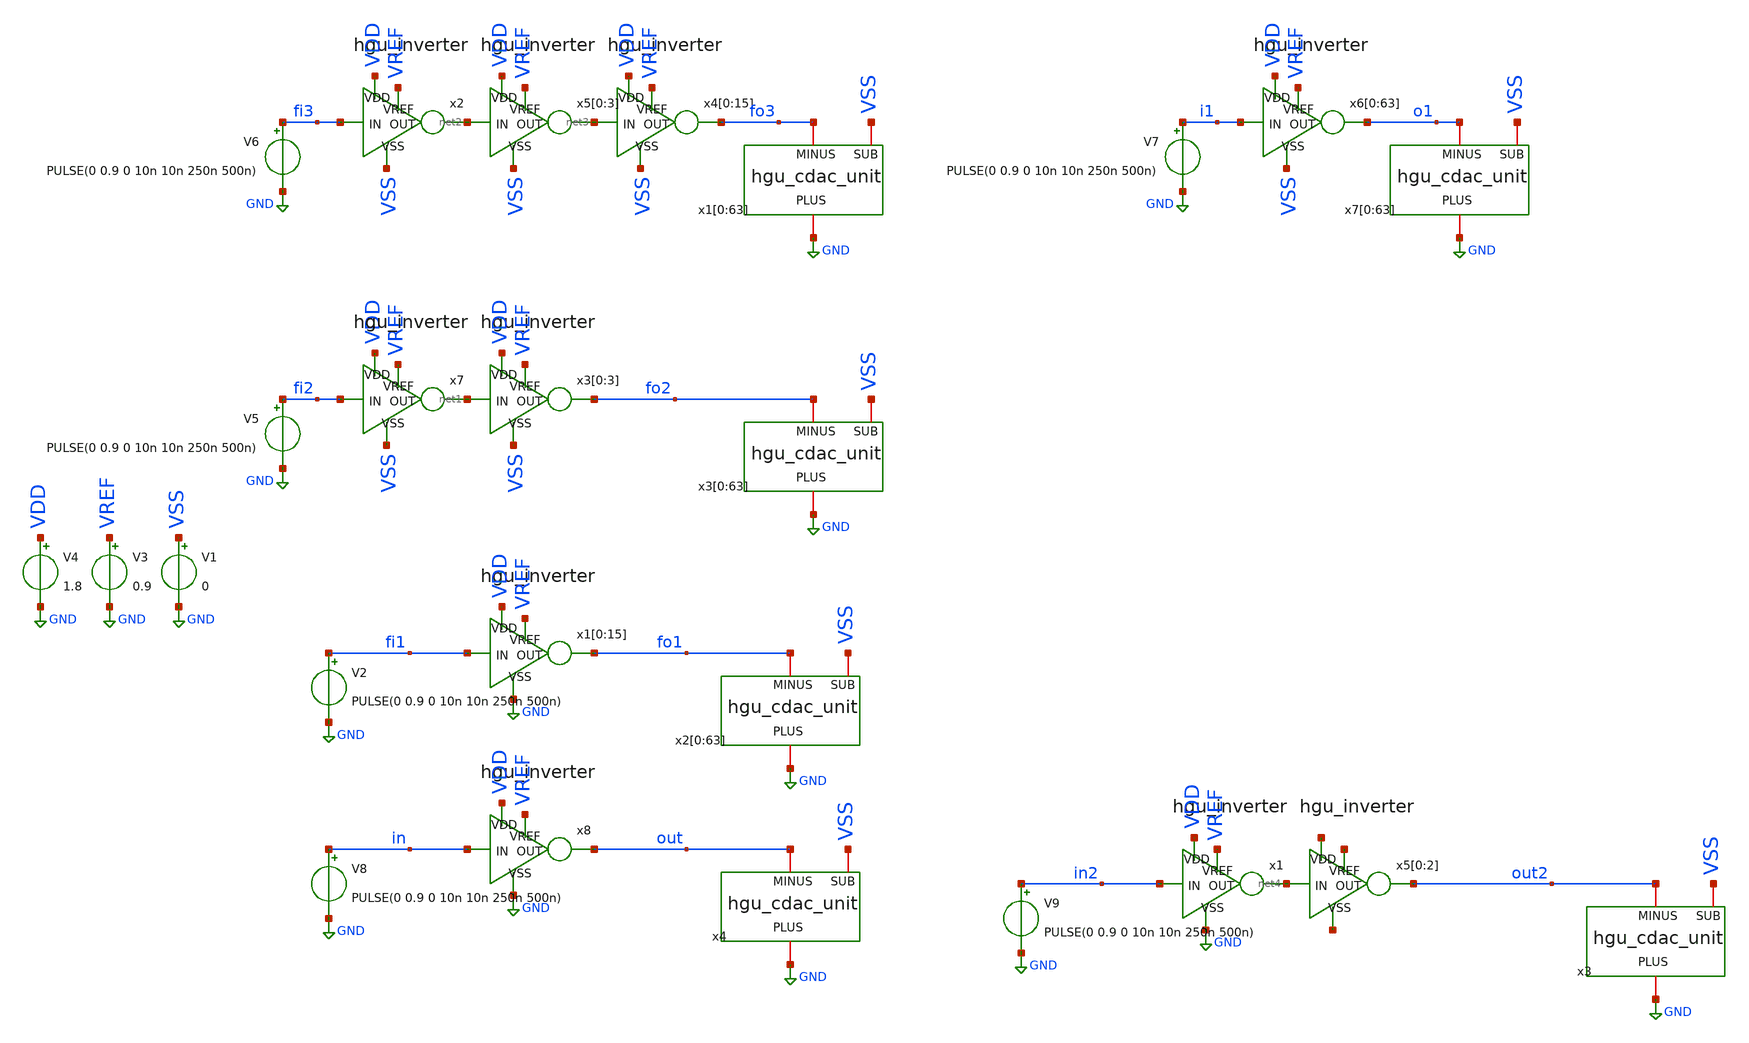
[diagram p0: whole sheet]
** sch_path: hgu/tb/tb_hgu_cdac_drv.sch
**.subckt tb_hgu_cdac_drv
x1[0] VDD fi1 fo1 GND VREF hgu_inverter
x1[1] VDD fi1 fo1 GND VREF hgu_inverter
x1[2] VDD fi1 fo1 GND VREF hgu_inverter
x1[3] VDD fi1 fo1 GND VREF hgu_inverter
x1[4] VDD fi1 fo1 GND VREF hgu_inverter
x1[5] VDD fi1 fo1 GND VREF hgu_inverter
x1[6] VDD fi1 fo1 GND VREF hgu_inverter
x1[7] VDD fi1 fo1 GND VREF hgu_inverter
x1[8] VDD fi1 fo1 GND VREF hgu_inverter
x1[9] VDD fi1 fo1 GND VREF hgu_inverter
x1[10] VDD fi1 fo1 GND VREF hgu_inverter
x1[11] VDD fi1 fo1 GND VREF hgu_inverter
x1[12] VDD fi1 fo1 GND VREF hgu_inverter
x1[13] VDD fi1 fo1 GND VREF hgu_inverter
x1[14] VDD fi1 fo1 GND VREF hgu_inverter
x1[15] VDD fi1 fo1 GND VREF hgu_inverter
x2[0] GND fo1 VSS hgu_cdac_unit
x2[1] GND fo1 VSS hgu_cdac_unit
x2[2] GND fo1 VSS hgu_cdac_unit
x2[3] GND fo1 VSS hgu_cdac_unit
x2[4] GND fo1 VSS hgu_cdac_unit
x2[5] GND fo1 VSS hgu_cdac_unit
x2[6] GND fo1 VSS hgu_cdac_unit
x2[7] GND fo1 VSS hgu_cdac_unit
x2[8] GND fo1 VSS hgu_cdac_unit
x2[9] GND fo1 VSS hgu_cdac_unit
x2[10] GND fo1 VSS hgu_cdac_unit
x2[11] GND fo1 VSS hgu_cdac_unit
x2[12] GND fo1 VSS hgu_cdac_unit
x2[13] GND fo1 VSS hgu_cdac_unit
x2[14] GND fo1 VSS hgu_cdac_unit
x2[15] GND fo1 VSS hgu_cdac_unit
x2[16] GND fo1 VSS hgu_cdac_unit
x2[17] GND fo1 VSS hgu_cdac_unit
x2[18] GND fo1 VSS hgu_cdac_unit
x2[19] GND fo1 VSS hgu_cdac_unit
x2[20] GND fo1 VSS hgu_cdac_unit
x2[21] GND fo1 VSS hgu_cdac_unit
x2[22] GND fo1 VSS hgu_cdac_unit
x2[23] GND fo1 VSS hgu_cdac_unit
x2[24] GND fo1 VSS hgu_cdac_unit
x2[25] GND fo1 VSS hgu_cdac_unit
x2[26] GND fo1 VSS hgu_cdac_unit
x2[27] GND fo1 VSS hgu_cdac_unit
x2[28] GND fo1 VSS hgu_cdac_unit
x2[29] GND fo1 VSS hgu_cdac_unit
x2[30] GND fo1 VSS hgu_cdac_unit
x2[31] GND fo1 VSS hgu_cdac_unit
x2[32] GND fo1 VSS hgu_cdac_unit
x2[33] GND fo1 VSS hgu_cdac_unit
x2[34] GND fo1 VSS hgu_cdac_unit
x2[35] GND fo1 VSS hgu_cdac_unit
x2[36] GND fo1 VSS hgu_cdac_unit
x2[37] GND fo1 VSS hgu_cdac_unit
x2[38] GND fo1 VSS hgu_cdac_unit
x2[39] GND fo1 VSS hgu_cdac_unit
x2[40] GND fo1 VSS hgu_cdac_unit
x2[41] GND fo1 VSS hgu_cdac_unit
x2[42] GND fo1 VSS hgu_cdac_unit
x2[43] GND fo1 VSS hgu_cdac_unit
x2[44] GND fo1 VSS hgu_cdac_unit
x2[45] GND fo1 VSS hgu_cdac_unit
x2[46] GND fo1 VSS hgu_cdac_unit
x2[47] GND fo1 VSS hgu_cdac_unit
x2[48] GND fo1 VSS hgu_cdac_unit
x2[49] GND fo1 VSS hgu_cdac_unit
x2[50] GND fo1 VSS hgu_cdac_unit
x2[51] GND fo1 VSS hgu_cdac_unit
x2[52] GND fo1 VSS hgu_cdac_unit
x2[53] GND fo1 VSS hgu_cdac_unit
x2[54] GND fo1 VSS hgu_cdac_unit
x2[55] GND fo1 VSS hgu_cdac_unit
x2[56] GND fo1 VSS hgu_cdac_unit
x2[57] GND fo1 VSS hgu_cdac_unit
x2[58] GND fo1 VSS hgu_cdac_unit
x2[59] GND fo1 VSS hgu_cdac_unit
x2[60] GND fo1 VSS hgu_cdac_unit
x2[61] GND fo1 VSS hgu_cdac_unit
x2[62] GND fo1 VSS hgu_cdac_unit
x2[63] GND fo1 VSS hgu_cdac_unit
V1 VSS GND 0
V2 fi1 GND PULSE(0 0.9 0 10n 10n 250n 500n)
V3 VREF GND 0.9
V4 VDD GND 1.8
x3[0] VDD net1 fo2 VSS VREF hgu_inverter
x3[1] VDD net1 fo2 VSS VREF hgu_inverter
x3[2] VDD net1 fo2 VSS VREF hgu_inverter
x3[3] VDD net1 fo2 VSS VREF hgu_inverter
x3[0] GND fo2 VSS hgu_cdac_unit
x3[1] GND fo2 VSS hgu_cdac_unit
x3[2] GND fo2 VSS hgu_cdac_unit
x3[3] GND fo2 VSS hgu_cdac_unit
x3[4] GND fo2 VSS hgu_cdac_unit
x3[5] GND fo2 VSS hgu_cdac_unit
x3[6] GND fo2 VSS hgu_cdac_unit
x3[7] GND fo2 VSS hgu_cdac_unit
x3[8] GND fo2 VSS hgu_cdac_unit
x3[9] GND fo2 VSS hgu_cdac_unit
x3[10] GND fo2 VSS hgu_cdac_unit
x3[11] GND fo2 VSS hgu_cdac_unit
x3[12] GND fo2 VSS hgu_cdac_unit
x3[13] GND fo2 VSS hgu_cdac_unit
x3[14] GND fo2 VSS hgu_cdac_unit
x3[15] GND fo2 VSS hgu_cdac_unit
x3[16] GND fo2 VSS hgu_cdac_unit
x3[17] GND fo2 VSS hgu_cdac_unit
x3[18] GND fo2 VSS hgu_cdac_unit
x3[19] GND fo2 VSS hgu_cdac_unit
x3[20] GND fo2 VSS hgu_cdac_unit
x3[21] GND fo2 VSS hgu_cdac_unit
x3[22] GND fo2 VSS hgu_cdac_unit
x3[23] GND fo2 VSS hgu_cdac_unit
x3[24] GND fo2 VSS hgu_cdac_unit
x3[25] GND fo2 VSS hgu_cdac_unit
x3[26] GND fo2 VSS hgu_cdac_unit
x3[27] GND fo2 VSS hgu_cdac_unit
x3[28] GND fo2 VSS hgu_cdac_unit
x3[29] GND fo2 VSS hgu_cdac_unit
x3[30] GND fo2 VSS hgu_cdac_unit
x3[31] GND fo2 VSS hgu_cdac_unit
x3[32] GND fo2 VSS hgu_cdac_unit
x3[33] GND fo2 VSS hgu_cdac_unit
x3[34] GND fo2 VSS hgu_cdac_unit
x3[35] GND fo2 VSS hgu_cdac_unit
x3[36] GND fo2 VSS hgu_cdac_unit
x3[37] GND fo2 VSS hgu_cdac_unit
x3[38] GND fo2 VSS hgu_cdac_unit
x3[39] GND fo2 VSS hgu_cdac_unit
x3[40] GND fo2 VSS hgu_cdac_unit
x3[41] GND fo2 VSS hgu_cdac_unit
x3[42] GND fo2 VSS hgu_cdac_unit
x3[43] GND fo2 VSS hgu_cdac_unit
x3[44] GND fo2 VSS hgu_cdac_unit
x3[45] GND fo2 VSS hgu_cdac_unit
x3[46] GND fo2 VSS hgu_cdac_unit
x3[47] GND fo2 VSS hgu_cdac_unit
x3[48] GND fo2 VSS hgu_cdac_unit
x3[49] GND fo2 VSS hgu_cdac_unit
x3[50] GND fo2 VSS hgu_cdac_unit
x3[51] GND fo2 VSS hgu_cdac_unit
x3[52] GND fo2 VSS hgu_cdac_unit
x3[53] GND fo2 VSS hgu_cdac_unit
x3[54] GND fo2 VSS hgu_cdac_unit
x3[55] GND fo2 VSS hgu_cdac_unit
x3[56] GND fo2 VSS hgu_cdac_unit
x3[57] GND fo2 VSS hgu_cdac_unit
x3[58] GND fo2 VSS hgu_cdac_unit
x3[59] GND fo2 VSS hgu_cdac_unit
x3[60] GND fo2 VSS hgu_cdac_unit
x3[61] GND fo2 VSS hgu_cdac_unit
x3[62] GND fo2 VSS hgu_cdac_unit
x3[63] GND fo2 VSS hgu_cdac_unit
V5 fi2 GND PULSE(0 0.9 0 10n 10n 250n 500n)
x5[0] VDD net2 net3[3] VSS VREF hgu_inverter
x5[1] VDD net2 net3[2] VSS VREF hgu_inverter
x5[2] VDD net2 net3[1] VSS VREF hgu_inverter
x5[3] VDD net2 net3[0] VSS VREF hgu_inverter
x2 VDD fi3 net2 VSS VREF hgu_inverter
x4[0] VDD net3[3] fo3 VSS VREF hgu_inverter
x4[1] VDD net3[2] fo3 VSS VREF hgu_inverter
x4[2] VDD net3[1] fo3 VSS VREF hgu_inverter
x4[3] VDD net3[0] fo3 VSS VREF hgu_inverter
x4[4] VDD net3[3] fo3 VSS VREF hgu_inverter
x4[5] VDD net3[2] fo3 VSS VREF hgu_inverter
x4[6] VDD net3[1] fo3 VSS VREF hgu_inverter
x4[7] VDD net3[0] fo3 VSS VREF hgu_inverter
x4[8] VDD net3[3] fo3 VSS VREF hgu_inverter
x4[9] VDD net3[2] fo3 VSS VREF hgu_inverter
x4[10] VDD net3[1] fo3 VSS VREF hgu_inverter
x4[11] VDD net3[0] fo3 VSS VREF hgu_inverter
x4[12] VDD net3[3] fo3 VSS VREF hgu_inverter
x4[13] VDD net3[2] fo3 VSS VREF hgu_inverter
x4[14] VDD net3[1] fo3 VSS VREF hgu_inverter
x4[15] VDD net3[0] fo3 VSS VREF hgu_inverter
x1[0] GND fo3 VSS hgu_cdac_unit
x1[1] GND fo3 VSS hgu_cdac_unit
x1[2] GND fo3 VSS hgu_cdac_unit
x1[3] GND fo3 VSS hgu_cdac_unit
x1[4] GND fo3 VSS hgu_cdac_unit
x1[5] GND fo3 VSS hgu_cdac_unit
x1[6] GND fo3 VSS hgu_cdac_unit
x1[7] GND fo3 VSS hgu_cdac_unit
x1[8] GND fo3 VSS hgu_cdac_unit
x1[9] GND fo3 VSS hgu_cdac_unit
x1[10] GND fo3 VSS hgu_cdac_unit
x1[11] GND fo3 VSS hgu_cdac_unit
x1[12] GND fo3 VSS hgu_cdac_unit
x1[13] GND fo3 VSS hgu_cdac_unit
x1[14] GND fo3 VSS hgu_cdac_unit
x1[15] GND fo3 VSS hgu_cdac_unit
x1[16] GND fo3 VSS hgu_cdac_unit
x1[17] GND fo3 VSS hgu_cdac_unit
x1[18] GND fo3 VSS hgu_cdac_unit
x1[19] GND fo3 VSS hgu_cdac_unit
x1[20] GND fo3 VSS hgu_cdac_unit
x1[21] GND fo3 VSS hgu_cdac_unit
x1[22] GND fo3 VSS hgu_cdac_unit
x1[23] GND fo3 VSS hgu_cdac_unit
x1[24] GND fo3 VSS hgu_cdac_unit
x1[25] GND fo3 VSS hgu_cdac_unit
x1[26] GND fo3 VSS hgu_cdac_unit
x1[27] GND fo3 VSS hgu_cdac_unit
x1[28] GND fo3 VSS hgu_cdac_unit
x1[29] GND fo3 VSS hgu_cdac_unit
x1[30] GND fo3 VSS hgu_cdac_unit
x1[31] GND fo3 VSS hgu_cdac_unit
x1[32] GND fo3 VSS hgu_cdac_unit
x1[33] GND fo3 VSS hgu_cdac_unit
x1[34] GND fo3 VSS hgu_cdac_unit
x1[35] GND fo3 VSS hgu_cdac_unit
x1[36] GND fo3 VSS hgu_cdac_unit
x1[37] GND fo3 VSS hgu_cdac_unit
x1[38] GND fo3 VSS hgu_cdac_unit
x1[39] GND fo3 VSS hgu_cdac_unit
x1[40] GND fo3 VSS hgu_cdac_unit
x1[41] GND fo3 VSS hgu_cdac_unit
x1[42] GND fo3 VSS hgu_cdac_unit
x1[43] GND fo3 VSS hgu_cdac_unit
x1[44] GND fo3 VSS hgu_cdac_unit
x1[45] GND fo3 VSS hgu_cdac_unit
x1[46] GND fo3 VSS hgu_cdac_unit
x1[47] GND fo3 VSS hgu_cdac_unit
x1[48] GND fo3 VSS hgu_cdac_unit
x1[49] GND fo3 VSS hgu_cdac_unit
x1[50] GND fo3 VSS hgu_cdac_unit
x1[51] GND fo3 VSS hgu_cdac_unit
x1[52] GND fo3 VSS hgu_cdac_unit
x1[53] GND fo3 VSS hgu_cdac_unit
x1[54] GND fo3 VSS hgu_cdac_unit
x1[55] GND fo3 VSS hgu_cdac_unit
x1[56] GND fo3 VSS hgu_cdac_unit
x1[57] GND fo3 VSS hgu_cdac_unit
x1[58] GND fo3 VSS hgu_cdac_unit
x1[59] GND fo3 VSS hgu_cdac_unit
x1[60] GND fo3 VSS hgu_cdac_unit
x1[61] GND fo3 VSS hgu_cdac_unit
x1[62] GND fo3 VSS hgu_cdac_unit
x1[63] GND fo3 VSS hgu_cdac_unit
V6 fi3 GND PULSE(0 0.9 0 10n 10n 250n 500n)
x6[0] VDD i1 o1 VSS VREF hgu_inverter
x6[1] VDD i1 o1 VSS VREF hgu_inverter
x6[2] VDD i1 o1 VSS VREF hgu_inverter
x6[3] VDD i1 o1 VSS VREF hgu_inverter
x6[4] VDD i1 o1 VSS VREF hgu_inverter
x6[5] VDD i1 o1 VSS VREF hgu_inverter
x6[6] VDD i1 o1 VSS VREF hgu_inverter
x6[7] VDD i1 o1 VSS VREF hgu_inverter
x6[8] VDD i1 o1 VSS VREF hgu_inverter
x6[9] VDD i1 o1 VSS VREF hgu_inverter
x6[10] VDD i1 o1 VSS VREF hgu_inverter
x6[11] VDD i1 o1 VSS VREF hgu_inverter
x6[12] VDD i1 o1 VSS VREF hgu_inverter
x6[13] VDD i1 o1 VSS VREF hgu_inverter
x6[14] VDD i1 o1 VSS VREF hgu_inverter
x6[15] VDD i1 o1 VSS VREF hgu_inverter
x6[16] VDD i1 o1 VSS VREF hgu_inverter
x6[17] VDD i1 o1 VSS VREF hgu_inverter
x6[18] VDD i1 o1 VSS VREF hgu_inverter
x6[19] VDD i1 o1 VSS VREF hgu_inverter
x6[20] VDD i1 o1 VSS VREF hgu_inverter
x6[21] VDD i1 o1 VSS VREF hgu_inverter
x6[22] VDD i1 o1 VSS VREF hgu_inverter
x6[23] VDD i1 o1 VSS VREF hgu_inverter
x6[24] VDD i1 o1 VSS VREF hgu_inverter
x6[25] VDD i1 o1 VSS VREF hgu_inverter
x6[26] VDD i1 o1 VSS VREF hgu_inverter
x6[27] VDD i1 o1 VSS VREF hgu_inverter
x6[28] VDD i1 o1 VSS VREF hgu_inverter
x6[29] VDD i1 o1 VSS VREF hgu_inverter
x6[30] VDD i1 o1 VSS VREF hgu_inverter
x6[31] VDD i1 o1 VSS VREF hgu_inverter
x6[32] VDD i1 o1 VSS VREF hgu_inverter
x6[33] VDD i1 o1 VSS VREF hgu_inverter
x6[34] VDD i1 o1 VSS VREF hgu_inverter
x6[35] VDD i1 o1 VSS VREF hgu_inverter
x6[36] VDD i1 o1 VSS VREF hgu_inverter
x6[37] VDD i1 o1 VSS VREF hgu_inverter
x6[38] VDD i1 o1 VSS VREF hgu_inverter
x6[39] VDD i1 o1 VSS VREF hgu_inverter
x6[40] VDD i1 o1 VSS VREF hgu_inverter
x6[41] VDD i1 o1 VSS VREF hgu_inverter
x6[42] VDD i1 o1 VSS VREF hgu_inverter
x6[43] VDD i1 o1 VSS VREF hgu_inverter
x6[44] VDD i1 o1 VSS VREF hgu_inverter
x6[45] VDD i1 o1 VSS VREF hgu_inverter
x6[46] VDD i1 o1 VSS VREF hgu_inverter
x6[47] VDD i1 o1 VSS VREF hgu_inverter
x6[48] VDD i1 o1 VSS VREF hgu_inverter
x6[49] VDD i1 o1 VSS VREF hgu_inverter
x6[50] VDD i1 o1 VSS VREF hgu_inverter
x6[51] VDD i1 o1 VSS VREF hgu_inverter
x6[52] VDD i1 o1 VSS VREF hgu_inverter
x6[53] VDD i1 o1 VSS VREF hgu_inverter
x6[54] VDD i1 o1 VSS VREF hgu_inverter
x6[55] VDD i1 o1 VSS VREF hgu_inverter
x6[56] VDD i1 o1 VSS VREF hgu_inverter
x6[57] VDD i1 o1 VSS VREF hgu_inverter
x6[58] VDD i1 o1 VSS VREF hgu_inverter
x6[59] VDD i1 o1 VSS VREF hgu_inverter
x6[60] VDD i1 o1 VSS VREF hgu_inverter
x6[61] VDD i1 o1 VSS VREF hgu_inverter
x6[62] VDD i1 o1 VSS VREF hgu_inverter
x6[63] VDD i1 o1 VSS VREF hgu_inverter
x7[0] GND o1 VSS hgu_cdac_unit
x7[1] GND o1 VSS hgu_cdac_unit
x7[2] GND o1 VSS hgu_cdac_unit
x7[3] GND o1 VSS hgu_cdac_unit
x7[4] GND o1 VSS hgu_cdac_unit
x7[5] GND o1 VSS hgu_cdac_unit
x7[6] GND o1 VSS hgu_cdac_unit
x7[7] GND o1 VSS hgu_cdac_unit
x7[8] GND o1 VSS hgu_cdac_unit
x7[9] GND o1 VSS hgu_cdac_unit
x7[10] GND o1 VSS hgu_cdac_unit
x7[11] GND o1 VSS hgu_cdac_unit
x7[12] GND o1 VSS hgu_cdac_unit
x7[13] GND o1 VSS hgu_cdac_unit
x7[14] GND o1 VSS hgu_cdac_unit
x7[15] GND o1 VSS hgu_cdac_unit
x7[16] GND o1 VSS hgu_cdac_unit
x7[17] GND o1 VSS hgu_cdac_unit
x7[18] GND o1 VSS hgu_cdac_unit
x7[19] GND o1 VSS hgu_cdac_unit
x7[20] GND o1 VSS hgu_cdac_unit
x7[21] GND o1 VSS hgu_cdac_unit
x7[22] GND o1 VSS hgu_cdac_unit
x7[23] GND o1 VSS hgu_cdac_unit
x7[24] GND o1 VSS hgu_cdac_unit
x7[25] GND o1 VSS hgu_cdac_unit
x7[26] GND o1 VSS hgu_cdac_unit
x7[27] GND o1 VSS hgu_cdac_unit
x7[28] GND o1 VSS hgu_cdac_unit
x7[29] GND o1 VSS hgu_cdac_unit
x7[30] GND o1 VSS hgu_cdac_unit
x7[31] GND o1 VSS hgu_cdac_unit
x7[32] GND o1 VSS hgu_cdac_unit
x7[33] GND o1 VSS hgu_cdac_unit
x7[34] GND o1 VSS hgu_cdac_unit
x7[35] GND o1 VSS hgu_cdac_unit
x7[36] GND o1 VSS hgu_cdac_unit
x7[37] GND o1 VSS hgu_cdac_unit
x7[38] GND o1 VSS hgu_cdac_unit
x7[39] GND o1 VSS hgu_cdac_unit
x7[40] GND o1 VSS hgu_cdac_unit
x7[41] GND o1 VSS hgu_cdac_unit
x7[42] GND o1 VSS hgu_cdac_unit
x7[43] GND o1 VSS hgu_cdac_unit
x7[44] GND o1 VSS hgu_cdac_unit
x7[45] GND o1 VSS hgu_cdac_unit
x7[46] GND o1 VSS hgu_cdac_unit
x7[47] GND o1 VSS hgu_cdac_unit
x7[48] GND o1 VSS hgu_cdac_unit
x7[49] GND o1 VSS hgu_cdac_unit
x7[50] GND o1 VSS hgu_cdac_unit
x7[51] GND o1 VSS hgu_cdac_unit
x7[52] GND o1 VSS hgu_cdac_unit
x7[53] GND o1 VSS hgu_cdac_unit
x7[54] GND o1 VSS hgu_cdac_unit
x7[55] GND o1 VSS hgu_cdac_unit
x7[56] GND o1 VSS hgu_cdac_unit
x7[57] GND o1 VSS hgu_cdac_unit
x7[58] GND o1 VSS hgu_cdac_unit
x7[59] GND o1 VSS hgu_cdac_unit
x7[60] GND o1 VSS hgu_cdac_unit
x7[61] GND o1 VSS hgu_cdac_unit
x7[62] GND o1 VSS hgu_cdac_unit
x7[63] GND o1 VSS hgu_cdac_unit
V7 i1 GND PULSE(0 0.9 0 10n 10n 250n 500n)
x7 VDD fi2 net1 VSS VREF hgu_inverter
x8 VDD in out GND VREF hgu_inverter
x4 GND out VSS hgu_cdac_unit
V8 in GND PULSE(0 0.9 0 10n 10n 250n 500n)
x1 VDD in2 net4 GND VREF hgu_inverter
x3 GND out2 VSS hgu_cdac_unit
V9 in2 GND PULSE(0 0.9 0 10n 10n 250n 500n)
x5[0] net5[2] net4 out2 net6[2] net7[2] hgu_inverter
x5[1] net5[1] net4 out2 net6[1] net7[1] hgu_inverter
x5[2] net5[0] net4 out2 net6[0] net7[0] hgu_inverter
**** begin user architecture code



.OPTIONS savecurrents
.tran 10ps 350ns
.include /foss/designs/hgu_goss/hgu/mag/hgu_cdac_unit.spice
.lib /foss/pdks/sky130A/libs.tech/ngspice/sky130.lib.spice tt
.include /foss/pdks/sky130A/libs.ref/sky130_fd_sc_hd/spice/sky130_fd_sc_hd.spice

.control
	run
	let svdd = 0.9
	let max = svdd*0.8
	let min = svdd*0.2
	let mid = svdd*0.5
	meas tran rising_sx1 find time when V(out)=min RISE=1 TD=1p
        meas tran rising_ex1 find time when V(out)=max RISE=1 TD=1p
        let rising_time_x1 = rising_ex1-rising_sx1
        meas tran falling_sx1 find time when V(out)=max FALL=1 TD=1p
        meas tran falling_ex1 find time when V(out)=min FALL=1 TD=1p
	let falling_time_x1 = falling_ex1-falling_sx1
	meas tran rising_sx3 find time when V(out2)=min RISE=1 TD=1p
        meas tran rising_ex3 find time when V(out2)=max RISE=1 TD=1p
        let rising_time_x3 = rising_ex1-rising_sx3
        meas tran falling_sx3 find time when V(out2)=max FALL=1 TD=1p
        meas tran falling_ex3 find time when V(out2)=min FALL=1 TD=1p
	let falling_time_x3 = falling_ex3-falling_sx3
	meas tran rising_s find time when V(o1)=min RISE=1 TD=1p
        meas tran rising_e find time when V(o1)=max RISE=1 TD=1p
        let rising_time = rising_e-rising_s
        meas tran falling_s find time when V(o1)=max FALL=1 TD=1p
        meas tran falling_e find time when V(o1)=min FALL=1 TD=1p
	let falling_time = falling_e-falling_s
	meas tran rising_s1 find time when V(fo1)=min RISE=1 TD=1p
        meas tran rising_e1 find time when V(fo1)=max RISE=1 TD=1p
        let rising_time1 = rising_e1-rising_s1
        meas tran falling_s1 find time when V(fo1)=max FALL=1 TD=1p
        meas tran falling_e1 find time when V(fo1)=min FALL=1 TD=1p
        let falling_time1 = falling_e1-falling_s1
	meas tran rising_s2 find time when V(fo2)=min RISE=1 TD=1p
        meas tran rising_e2 find time when V(fo2)=max RISE=1 TD=1p
        let rising_time2 = rising_e2-rising_s2
        meas tran falling_s2 find time when V(fo2)=max FALL=1 TD=1p
        meas tran falling_e2 find time when V(fo2)=min FALL=1 TD=1p
        let falling_time2 = falling_e2-falling_s2
	meas tran rising_s3 find time when V(fo1)=min RISE=1 TD=1p
        meas tran rising_e3 find time when V(fo1)=max RISE=1 TD=1p
        let rising_time3 = rising_e3-rising_s3
        meas tran falling_s3 find time when V(fo3)=max FALL=1 TD=1p
        meas tran falling_e3 find time when V(fo3)=min FALL=1 TD=1p
        let falling_time3 = falling_e3-falling_s3

        print rising_time_x1 falling_time_x1 rising_time_x3 falling_time_x3 rising_time falling_time
+ rising_time1 falling_time1 rising_time2 falling_time2 rising_time3 falling_time3
	plot V(fi1) V(fo1)
	plot V(fi2) V(fo2)
	plot V(fi3) V(fo3)
	plot V(i1) V(o1)
	plot V(in) V(out)

.endc
.save all



**** end user architecture code
**.ends
.GLOBAL GND
.end
